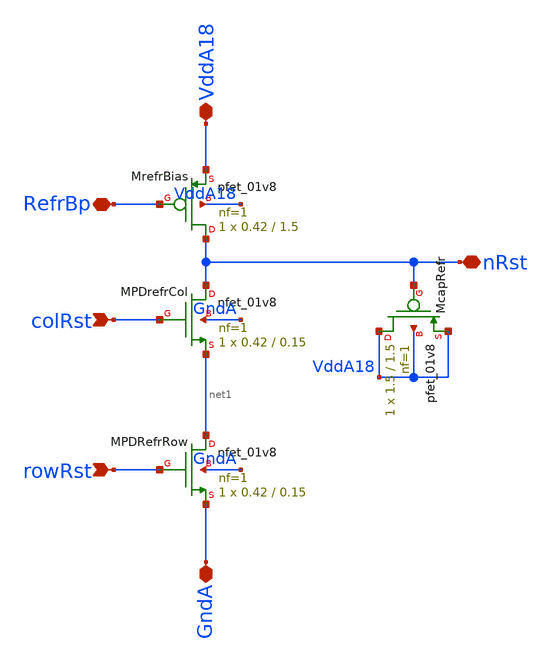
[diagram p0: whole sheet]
** sch_path: analog/klayout/production/final_merge_20260923/testbenches/cace/analog/xschem/PixelResetGen.sch
**.subckt PixelResetGen rowRst colRst RefrBp GndA VddA18 nRst
*.ipin rowRst
*.ipin colRst
*.iopin RefrBp
*.iopin GndA
*.iopin VddA18
*.iopin nRst
XMPDrefrCol nRst colRst net1 GndA sky130_fd_pr__nfet_01v8 L=0.15 W=0.42 nf=1 ad='int((1 + 1)/2) * 0.42 / 1 * 0.29'
+ as='int((1 + 2)/2) * 0.42 / 1 * 0.29' pd='2*int((1 + 1)/2) * (0.42 / 1 + 0.29)' ps='2*int((1 + 2)/2) * (0.42 / 1 + 0.29)'
+ nrd='0.29 / 0.42 ' nrs='0.29 / 0.42 ' sa=0 sb=0 sd=0 mult=1 m=1
XMrefrBias nRst RefrBp VddA18 VddA18 sky130_fd_pr__pfet_01v8 L=1.5 W=0.42 nf=1 ad='int((1 + 1)/2) * 0.42 / 1 * 0.29'
+ as='int((1 + 2)/2) * 0.42 / 1 * 0.29' pd='2*int((1 + 1)/2) * (0.42 / 1 + 0.29)' ps='2*int((1 + 2)/2) * (0.42 / 1 + 0.29)'
+ nrd='0.29 / 0.42 ' nrs='0.29 / 0.42 ' sa=0 sb=0 sd=0 mult=1 m=1
XMcapRefr VddA18 nRst VddA18 VddA18 sky130_fd_pr__pfet_01v8 L=1.5 W=1.5 nf=1 ad='int((1 + 1)/2) * 1.5 / 1 * 0.29'
+ as='int((1 + 2)/2) * 1.5 / 1 * 0.29' pd='2*int((1 + 1)/2) * (1.5 / 1 + 0.29)' ps='2*int((1 + 2)/2) * (1.5 / 1 + 0.29)'
+ nrd='0.29 / 1.5 ' nrs='0.29 / 1.5 ' sa=0 sb=0 sd=0 mult=1 m=1
XMPDRefrRow net1 rowRst GndA GndA sky130_fd_pr__nfet_01v8 L=0.15 W=0.42 nf=1 ad='int((1 + 1)/2) * 0.42 / 1 * 0.29'
+ as='int((1 + 2)/2) * 0.42 / 1 * 0.29' pd='2*int((1 + 1)/2) * (0.42 / 1 + 0.29)' ps='2*int((1 + 2)/2) * (0.42 / 1 + 0.29)'
+ nrd='0.29 / 0.42 ' nrs='0.29 / 0.42 ' sa=0 sb=0 sd=0 mult=1 m=1
**.ends
.end
